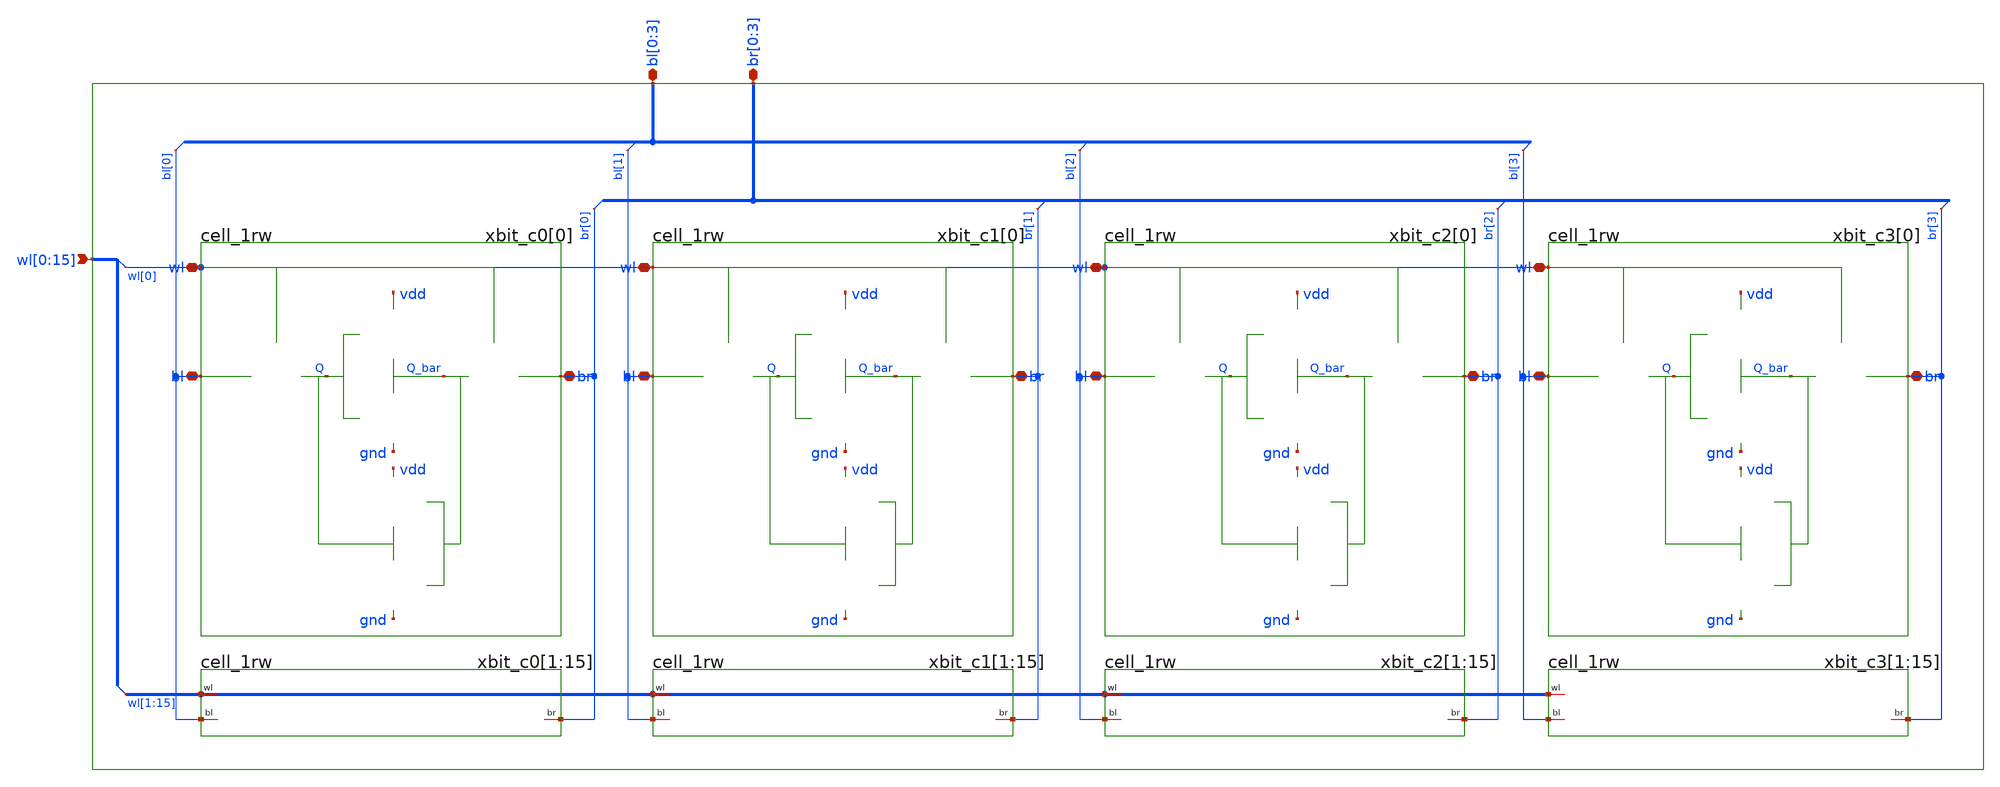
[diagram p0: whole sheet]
** sch_path: sram_4_16_scn4m/bitcell_array.sch
**.subckt bitcell_array bl[0],bl[1],bl[2],bl[3]
*+ wl[0],wl[1],wl[2],wl[3],wl[4],wl[5],wl[6],wl[7],wl[8],wl[9],wl[10],wl[11],wl[12],wl[13],wl[14],wl[15] br[0],br[1],br[2],br[3]
*.iopin bl[0],bl[1],bl[2],bl[3]
*.ipin
*+ wl[0],wl[1],wl[2],wl[3],wl[4],wl[5],wl[6],wl[7],wl[8],wl[9],wl[10],wl[11],wl[12],wl[13],wl[14],wl[15]
*.iopin br[0],br[1],br[2],br[3]
xbit_c0[1] bl[0] br[0] wl[1] vdd gnd cell_1rw
xbit_c0[2] bl[0] br[0] wl[2] vdd gnd cell_1rw
xbit_c0[3] bl[0] br[0] wl[3] vdd gnd cell_1rw
xbit_c0[4] bl[0] br[0] wl[4] vdd gnd cell_1rw
xbit_c0[5] bl[0] br[0] wl[5] vdd gnd cell_1rw
xbit_c0[6] bl[0] br[0] wl[6] vdd gnd cell_1rw
xbit_c0[7] bl[0] br[0] wl[7] vdd gnd cell_1rw
xbit_c0[8] bl[0] br[0] wl[8] vdd gnd cell_1rw
xbit_c0[9] bl[0] br[0] wl[9] vdd gnd cell_1rw
xbit_c0[10] bl[0] br[0] wl[10] vdd gnd cell_1rw
xbit_c0[11] bl[0] br[0] wl[11] vdd gnd cell_1rw
xbit_c0[12] bl[0] br[0] wl[12] vdd gnd cell_1rw
xbit_c0[13] bl[0] br[0] wl[13] vdd gnd cell_1rw
xbit_c0[14] bl[0] br[0] wl[14] vdd gnd cell_1rw
xbit_c0[15] bl[0] br[0] wl[15] vdd gnd cell_1rw
xbit_c0[0] bl[0] br[0] wl[0] vdd gnd cell_1rw
xbit_c1[1] bl[1] br[1] wl[1] vdd gnd cell_1rw
xbit_c1[2] bl[1] br[1] wl[2] vdd gnd cell_1rw
xbit_c1[3] bl[1] br[1] wl[3] vdd gnd cell_1rw
xbit_c1[4] bl[1] br[1] wl[4] vdd gnd cell_1rw
xbit_c1[5] bl[1] br[1] wl[5] vdd gnd cell_1rw
xbit_c1[6] bl[1] br[1] wl[6] vdd gnd cell_1rw
xbit_c1[7] bl[1] br[1] wl[7] vdd gnd cell_1rw
xbit_c1[8] bl[1] br[1] wl[8] vdd gnd cell_1rw
xbit_c1[9] bl[1] br[1] wl[9] vdd gnd cell_1rw
xbit_c1[10] bl[1] br[1] wl[10] vdd gnd cell_1rw
xbit_c1[11] bl[1] br[1] wl[11] vdd gnd cell_1rw
xbit_c1[12] bl[1] br[1] wl[12] vdd gnd cell_1rw
xbit_c1[13] bl[1] br[1] wl[13] vdd gnd cell_1rw
xbit_c1[14] bl[1] br[1] wl[14] vdd gnd cell_1rw
xbit_c1[15] bl[1] br[1] wl[15] vdd gnd cell_1rw
xbit_c1[0] bl[1] br[1] wl[0] vdd gnd cell_1rw
xbit_c2[1] bl[2] br[2] wl[1] vdd gnd cell_1rw
xbit_c2[2] bl[2] br[2] wl[2] vdd gnd cell_1rw
xbit_c2[3] bl[2] br[2] wl[3] vdd gnd cell_1rw
xbit_c2[4] bl[2] br[2] wl[4] vdd gnd cell_1rw
xbit_c2[5] bl[2] br[2] wl[5] vdd gnd cell_1rw
xbit_c2[6] bl[2] br[2] wl[6] vdd gnd cell_1rw
xbit_c2[7] bl[2] br[2] wl[7] vdd gnd cell_1rw
xbit_c2[8] bl[2] br[2] wl[8] vdd gnd cell_1rw
xbit_c2[9] bl[2] br[2] wl[9] vdd gnd cell_1rw
xbit_c2[10] bl[2] br[2] wl[10] vdd gnd cell_1rw
xbit_c2[11] bl[2] br[2] wl[11] vdd gnd cell_1rw
xbit_c2[12] bl[2] br[2] wl[12] vdd gnd cell_1rw
xbit_c2[13] bl[2] br[2] wl[13] vdd gnd cell_1rw
xbit_c2[14] bl[2] br[2] wl[14] vdd gnd cell_1rw
xbit_c2[15] bl[2] br[2] wl[15] vdd gnd cell_1rw
xbit_c2[0] bl[2] br[2] wl[0] vdd gnd cell_1rw
xbit_c3[1] bl[3] br[3] wl[1] vdd gnd cell_1rw
xbit_c3[2] bl[3] br[3] wl[2] vdd gnd cell_1rw
xbit_c3[3] bl[3] br[3] wl[3] vdd gnd cell_1rw
xbit_c3[4] bl[3] br[3] wl[4] vdd gnd cell_1rw
xbit_c3[5] bl[3] br[3] wl[5] vdd gnd cell_1rw
xbit_c3[6] bl[3] br[3] wl[6] vdd gnd cell_1rw
xbit_c3[7] bl[3] br[3] wl[7] vdd gnd cell_1rw
xbit_c3[8] bl[3] br[3] wl[8] vdd gnd cell_1rw
xbit_c3[9] bl[3] br[3] wl[9] vdd gnd cell_1rw
xbit_c3[10] bl[3] br[3] wl[10] vdd gnd cell_1rw
xbit_c3[11] bl[3] br[3] wl[11] vdd gnd cell_1rw
xbit_c3[12] bl[3] br[3] wl[12] vdd gnd cell_1rw
xbit_c3[13] bl[3] br[3] wl[13] vdd gnd cell_1rw
xbit_c3[14] bl[3] br[3] wl[14] vdd gnd cell_1rw
xbit_c3[15] bl[3] br[3] wl[15] vdd gnd cell_1rw
xbit_c3[0] bl[3] br[3] wl[0] vdd gnd cell_1rw
**.ends

* expanding   symbol:  cell_1rw.sym # of pins=3
** sym_path: sram_4_16_scn4m/cell_1rw.sym
** sch_path: sram_4_16_scn4m/cell_1rw.sch
.subckt cell_1rw bl br wl vdd gnd
*.iopin bl
*.iopin br
*.iopin wl
XM1004 Q wl bl gnd sky130_fd_pr__nfet_01v8 L=0.4 W=0.8 nf=1 ad='int((nf+1)/2) * W/nf * 0.29' as='int((nf+2)/2) * W/nf * 0.29'
+ pd='2*int((nf+1)/2) * (W/nf + 0.29)' ps='2*int((nf+2)/2) * (W/nf + 0.29)' nrd='0.29 / W' nrs='0.29 / W'
+ sa=0 sb=0 sd=0 mult=1 m=1
XM1001 Q_bar Q vdd vdd sky130_fd_pr__pfet_01v8 L=0.8 W=0.6 nf=1 ad='int((nf+1)/2) * W/nf * 0.29' as='int((nf+2)/2) * W/nf * 0.29'
+ pd='2*int((nf+1)/2) * (W/nf + 0.29)' ps='2*int((nf+2)/2) * (W/nf + 0.29)' nrd='0.29 / W' nrs='0.29 / W'
+ sa=0 sb=0 sd=0 mult=1 m=1
XM1003 Q_bar Q gnd gnd sky130_fd_pr__nfet_01v8 L=0.4 W=1.6 nf=1 ad='int((nf+1)/2) * W/nf * 0.29' as='int((nf+2)/2) * W/nf * 0.29'
+ pd='2*int((nf+1)/2) * (W/nf + 0.29)' ps='2*int((nf+2)/2) * (W/nf + 0.29)' nrd='0.29 / W' nrs='0.29 / W'
+ sa=0 sb=0 sd=0 mult=1 m=1
XM1002 Q Q_bar gnd gnd sky130_fd_pr__nfet_01v8 L=0.4 W=1.6 nf=1 ad='int((nf+1)/2) * W/nf * 0.29' as='int((nf+2)/2) * W/nf * 0.29'
+ pd='2*int((nf+1)/2) * (W/nf + 0.29)' ps='2*int((nf+2)/2) * (W/nf + 0.29)' nrd='0.29 / W' nrs='0.29 / W'
+ sa=0 sb=0 sd=0 mult=1 m=1
XM1000 Q Q_bar vdd vdd sky130_fd_pr__pfet_01v8 L=0.8 W=0.6 nf=1 ad='int((nf+1)/2) * W/nf * 0.29' as='int((nf+2)/2) * W/nf * 0.29'
+ pd='2*int((nf+1)/2) * (W/nf + 0.29)' ps='2*int((nf+2)/2) * (W/nf + 0.29)' nrd='0.29 / W' nrs='0.29 / W'
+ sa=0 sb=0 sd=0 mult=1 m=1
XM1005 br wl Q_bar gnd sky130_fd_pr__nfet_01v8 L=0.4 W=0.8 nf=1 ad='int((nf+1)/2) * W/nf * 0.29' as='int((nf+2)/2) * W/nf * 0.29'
+ pd='2*int((nf+1)/2) * (W/nf + 0.29)' ps='2*int((nf+2)/2) * (W/nf + 0.29)' nrd='0.29 / W' nrs='0.29 / W'
+ sa=0 sb=0 sd=0 mult=1 m=1
.ends

.end
